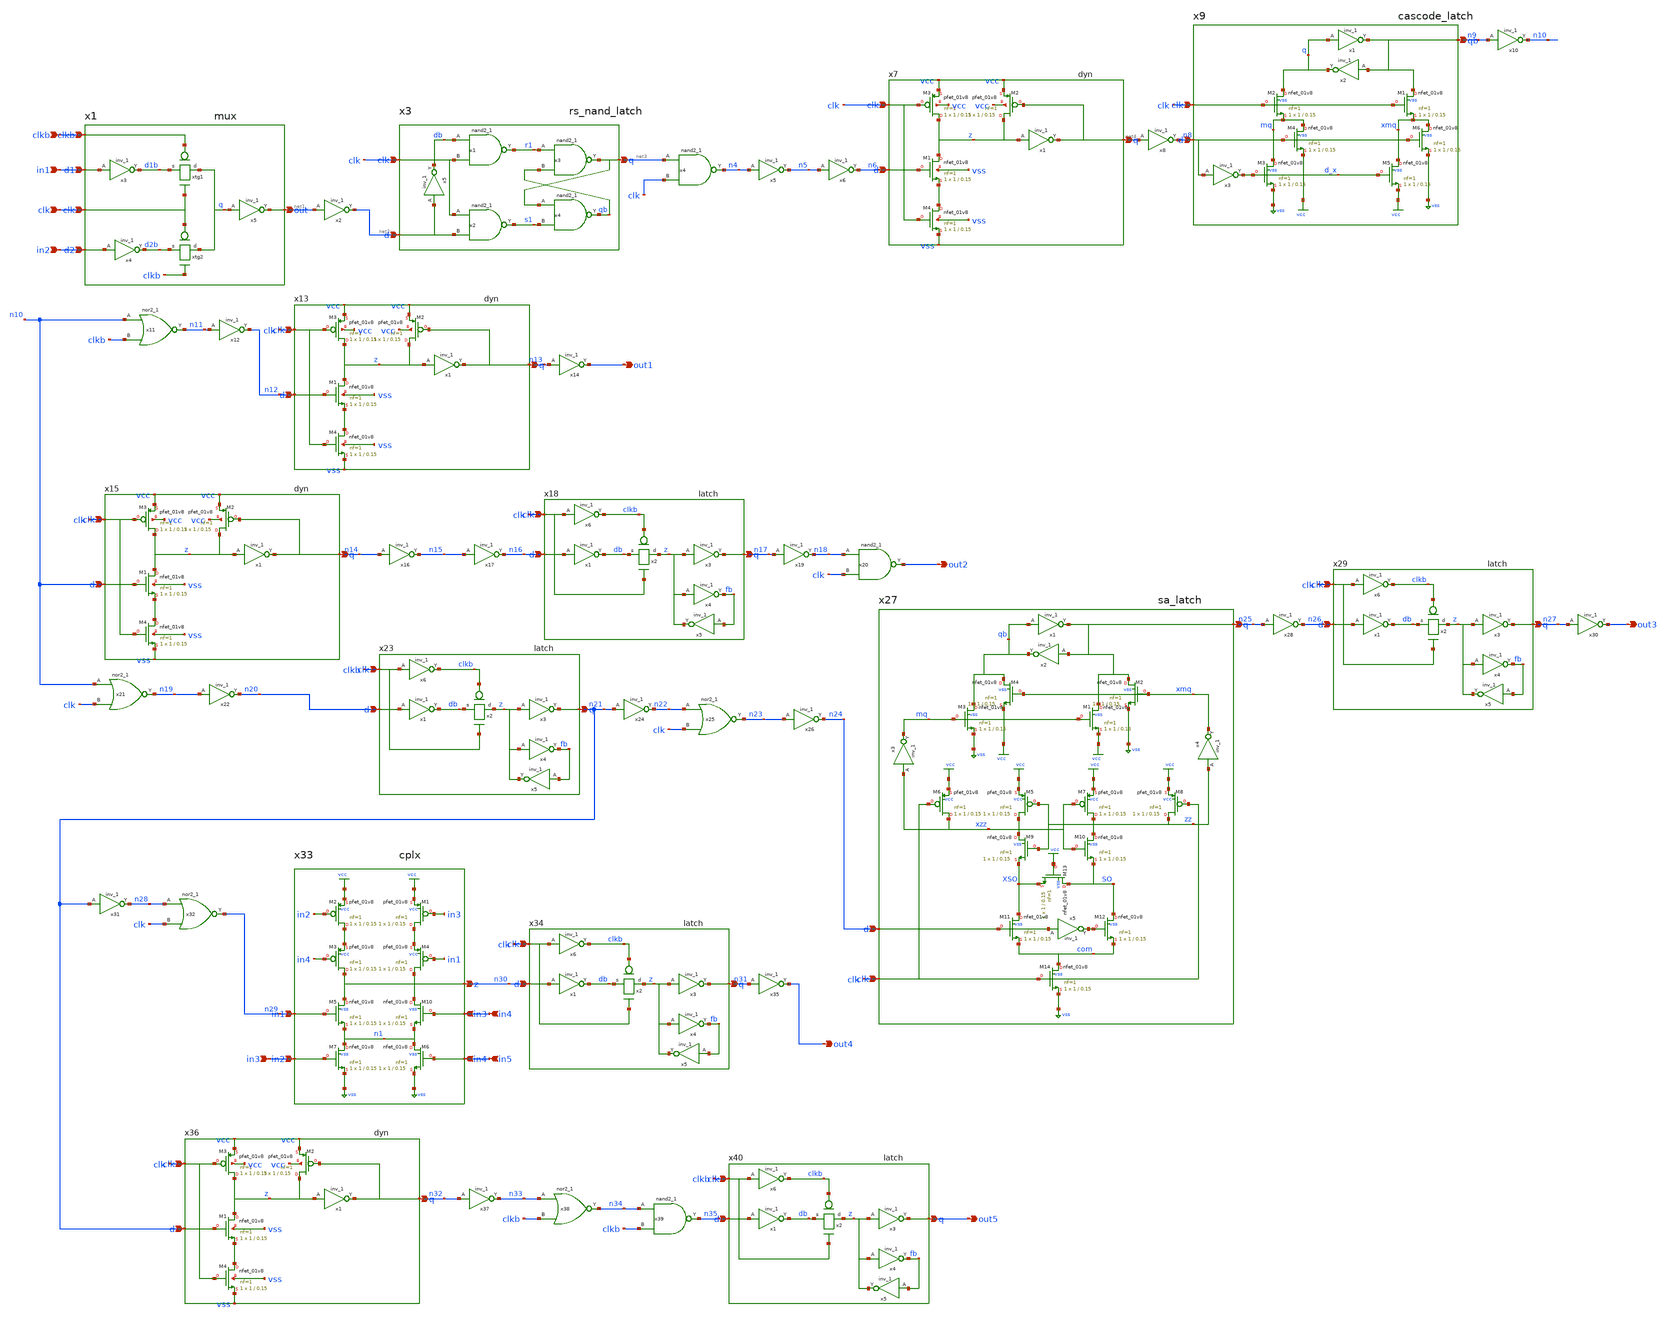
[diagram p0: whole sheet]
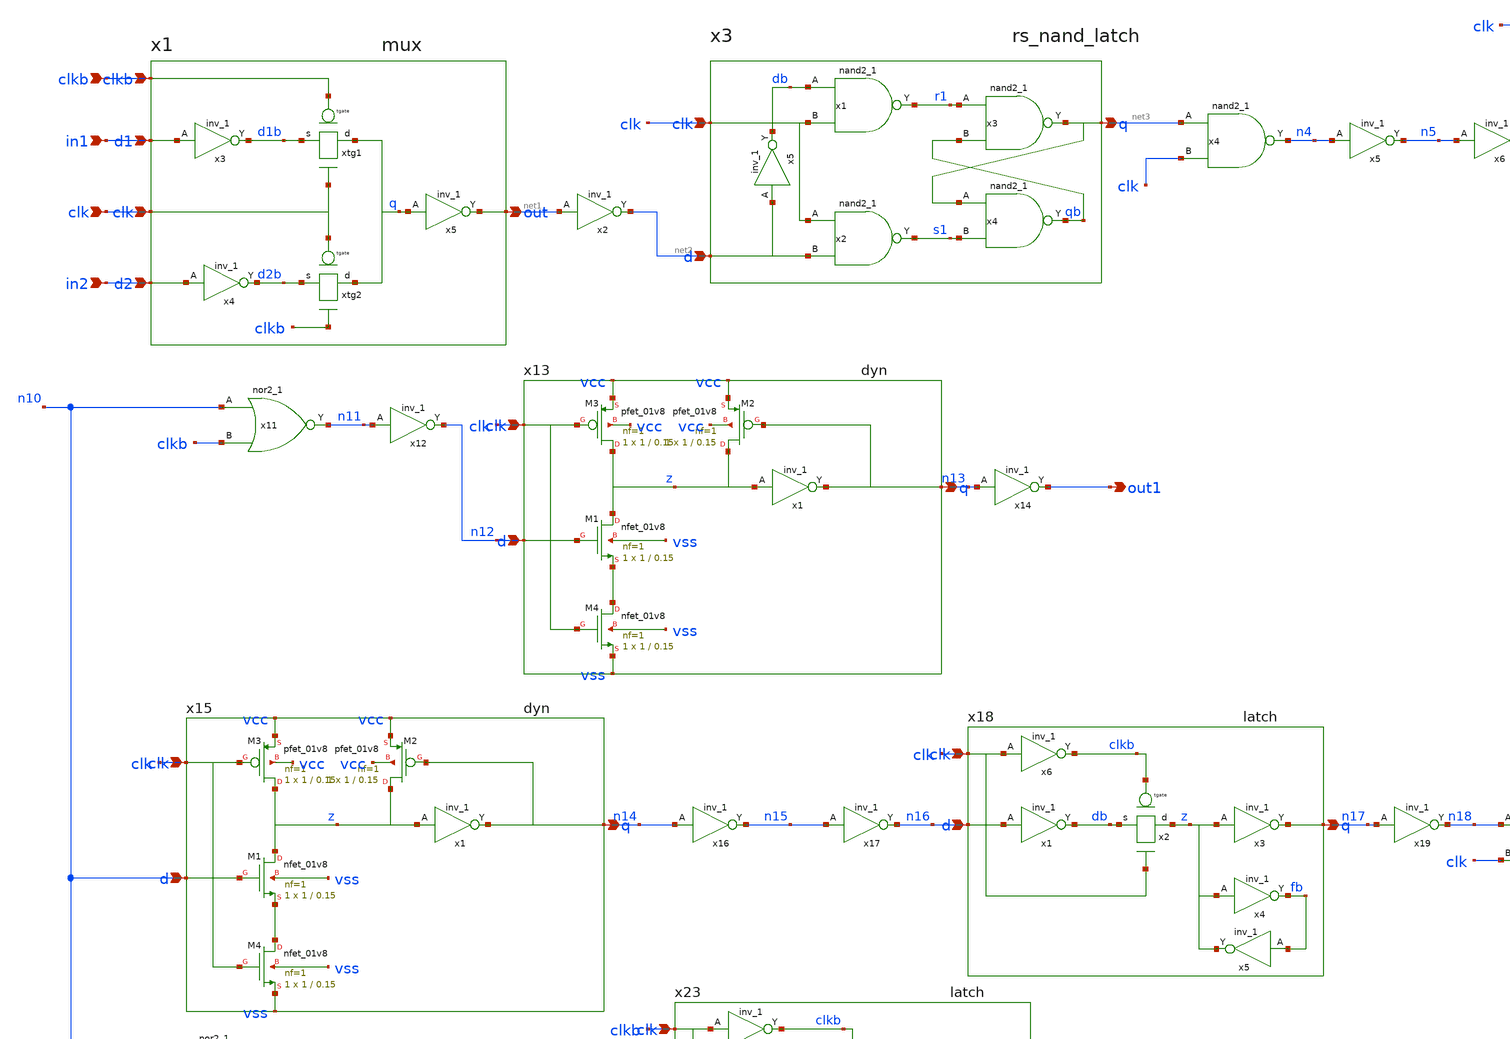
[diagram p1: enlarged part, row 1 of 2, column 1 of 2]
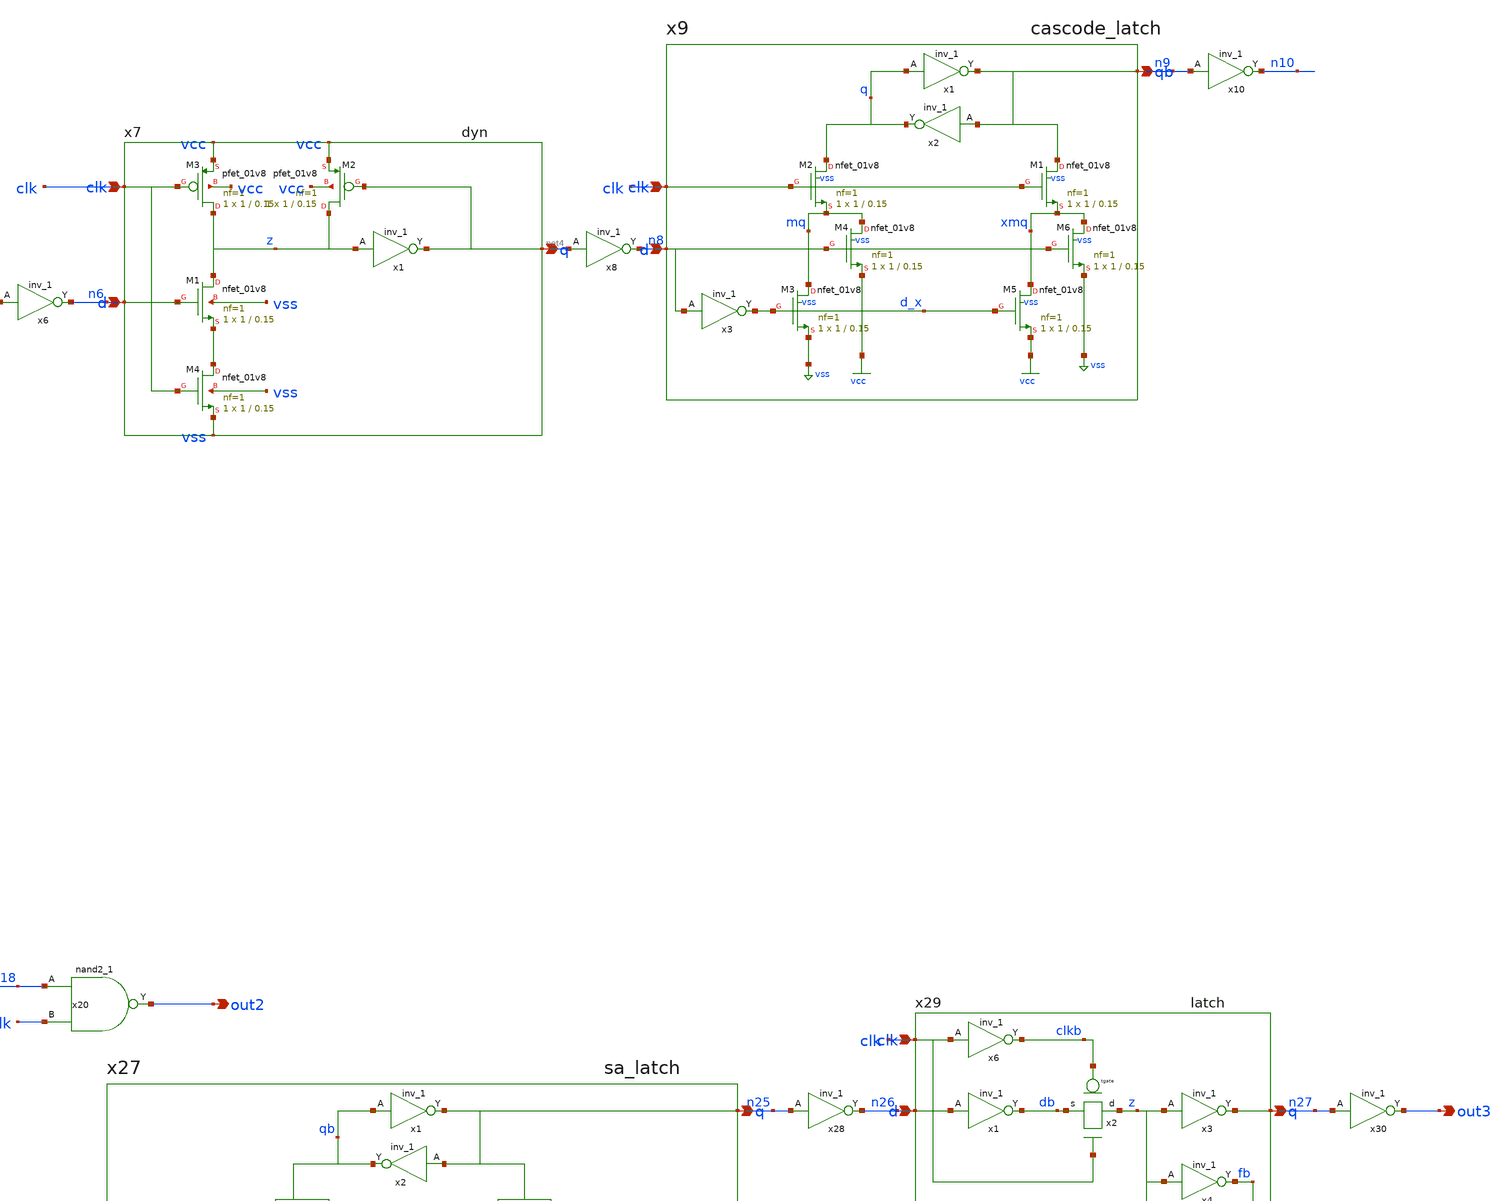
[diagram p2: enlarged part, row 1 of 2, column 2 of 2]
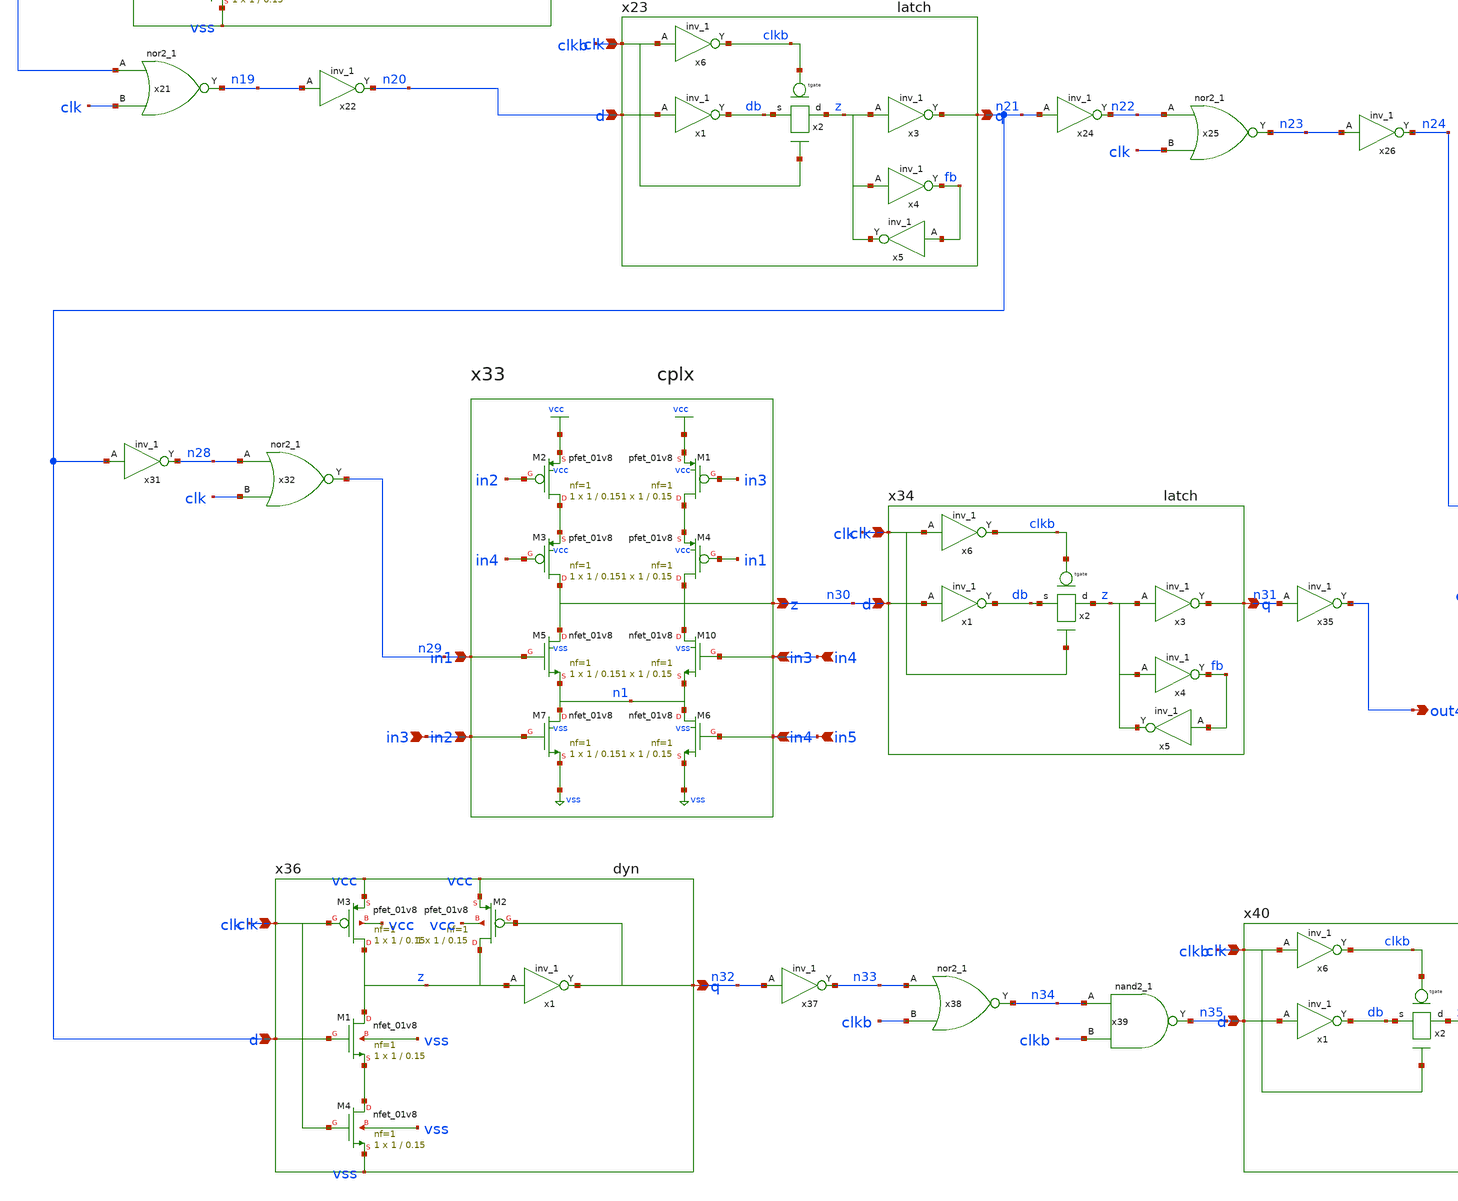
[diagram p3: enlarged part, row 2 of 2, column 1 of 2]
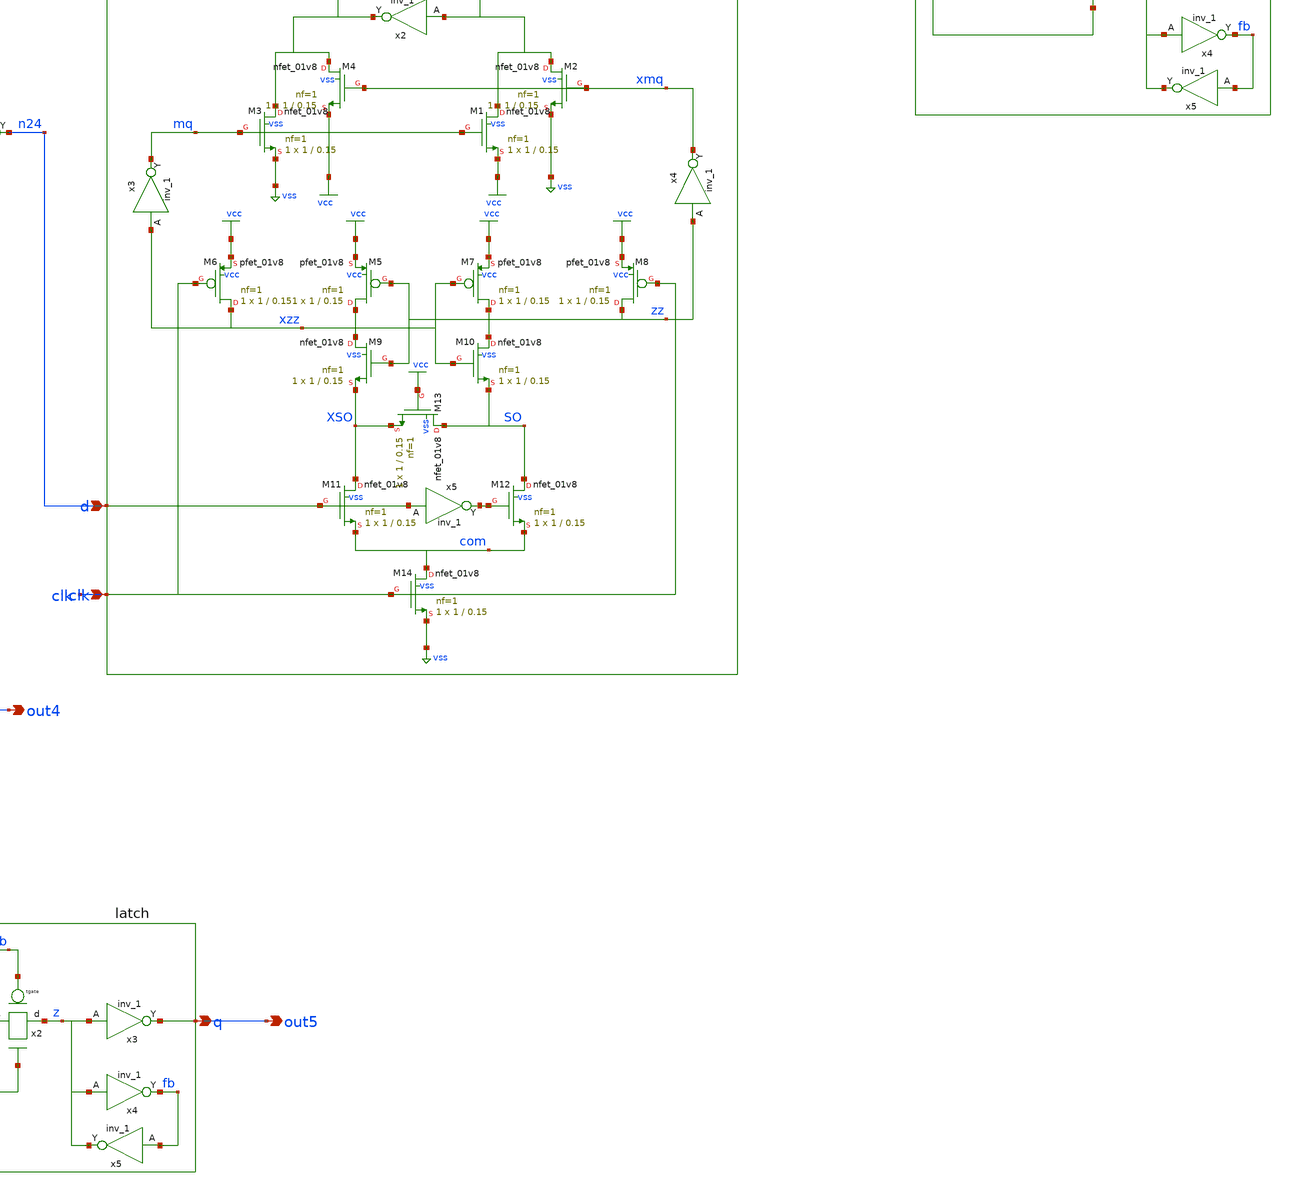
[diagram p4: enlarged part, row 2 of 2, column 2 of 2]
** sch_path: src/xe/test_cases/yxt_input_rel_test4.sch
**.subckt yxt_input_rel_test4 clkb in1 clk in2 out1 out2 out3 in3 in4 in5 out4 out5
*.ipin clkb
*.ipin in1
*.ipin clk
*.ipin in2
*.opin out1
*.opin out2
*.opin out3
*.ipin in3
*.ipin in4
*.ipin in5
*.opin out4
*.opin out5
x1 in1 in2 net1 clkb clk vcc vss mux
x2 net1 vss vss vcc vcc net2 sky130_fd_sc_hd__inv_1
x3 clk net2 net3 vcc vss rs_nand_latch
x4 net3 clk vss vss vcc vcc n4 sky130_fd_sc_hd__nand2_1
x5 n4 vss vss vcc vcc n5 sky130_fd_sc_hd__inv_1
x6 n5 vss vss vcc vcc n6 sky130_fd_sc_hd__inv_1
x7 clk net4 n6 vcc vss dyn
x8 net4 vss vss vcc vcc n8 sky130_fd_sc_hd__inv_1
x9 n8 clk n9 vcc vss cascode_latch
x10 n9 vss vss vcc vcc n10 sky130_fd_sc_hd__inv_1
x11 n10 clkb vss vss vcc vcc n11 sky130_fd_sc_hd__nor2_1
x12 n11 vss vss vcc vcc n12 sky130_fd_sc_hd__inv_1
x13 clk n13 n12 vcc vss dyn
x14 n13 vss vss vcc vcc out1 sky130_fd_sc_hd__inv_1
x15 clk n14 n10 vcc vss dyn
x16 n14 vss vss vcc vcc n15 sky130_fd_sc_hd__inv_1
x17 n15 vss vss vcc vcc n16 sky130_fd_sc_hd__inv_1
x18 clk n17 n16 vcc vss latch
x19 n17 vss vss vcc vcc n18 sky130_fd_sc_hd__inv_1
x20 n18 clk vss vss vcc vcc out2 sky130_fd_sc_hd__nand2_1
x21 n10 clk vss vss vcc vcc n19 sky130_fd_sc_hd__nor2_1
x22 n19 vss vss vcc vcc n20 sky130_fd_sc_hd__inv_1
x23 clkb n21 n20 vcc vss latch
x24 n21 vss vss vcc vcc n22 sky130_fd_sc_hd__inv_1
x25 n22 clk vss vss vcc vcc n23 sky130_fd_sc_hd__nor2_1
x26 n23 vss vss vcc vcc n24 sky130_fd_sc_hd__inv_1
x27 clk n25 n24 vcc vss sa_latch
x28 n25 vss vss vcc vcc n26 sky130_fd_sc_hd__inv_1
x29 clk n27 n26 vcc vss latch
x30 n27 vss vss vcc vcc out3 sky130_fd_sc_hd__inv_1
x33 n29 in3 in4 in5 n30 vcc vss cplx
x32 n28 clk vss vss vcc vcc n29 sky130_fd_sc_hd__nor2_1
x31 n21 vss vss vcc vcc n28 sky130_fd_sc_hd__inv_1
x34 clk n31 n30 vcc vss latch
x35 n31 vss vss vcc vcc out4 sky130_fd_sc_hd__inv_1
x36 clk n32 n21 vcc vss dyn
x37 n32 vss vss vcc vcc n33 sky130_fd_sc_hd__inv_1
x38 n33 clkb vss vss vcc vcc n34 sky130_fd_sc_hd__nor2_1
x39 n34 clkb vss vss vcc vcc n35 sky130_fd_sc_hd__nand2_1
x40 clkb out5 n35 vcc vss latch
**** begin user architecture code

** opencircuitdesign pdks install

.subckt sky130_fd_sc_hd__inv_1 A VGND VNB VPB VPWR Y
M0 VGND A Y VNB sky130_fd_pr__nfet_01v8 w=650000u l=150000u
M1 VPWR A Y VPB sky130_fd_pr__pfet_01v8_hvt w=1e+06u l=150000u
.ends

.subckt sky130_fd_sc_hd__nand2_1 A B VGND VNB VPB VPWR Y
M0 Y A VPWR VPB sky130_fd_pr__pfet_01v8_hvt w=1e+06u l=150000u
M1 VPWR B Y VPB sky130_fd_pr__pfet_01v8_hvt w=1e+06u l=150000u
M2 VGND B a_113_47# VNB sky130_fd_pr__nfet_01v8 w=650000u l=150000u
M3 a_113_47# A Y VNB sky130_fd_pr__nfet_01v8 w=650000u l=150000u
.ends

.SUBCKT sky130_fd_sc_hd__nor2_1 A B VGND VNB VPB VPWR Y
*.PININFO A:I B:I VGND:I VNB:I VPB:I VPWR:I Y:O
MMP0 VPWR A sndPA VPB sky130_fd_pr__pfet_01v8_hvt m=1 w=1.0 l=0.15 mult=1 sa=0.265  sb=0.265 sd=0.28
+ topography=normal area=0.063 perim=1.14
MMP1 sndPA B Y VPB sky130_fd_pr__pfet_01v8_hvt m=1 w=1.0 l=0.15 mult=1 sa=0.265  sb=0.265 sd=0.28
+ topography=normal area=0.063 perim=1.14
MMN0 Y A VGND VNB sky130_fd_pr__nfet_01v8 m=1 w=0.65 l=0.15 mult=1 sa=0.265 sb=0.265  sd=0.28
+ topography=normal area=0.063 perim=1.14
MMN1 Y B VGND VNB sky130_fd_pr__nfet_01v8 m=1 w=0.65 l=0.15 mult=1 sa=0.265 sb=0.265  sd=0.28
+ topography=normal area=0.063 perim=1.14
.ENDS sky130_fd_sc_hd__nor2_1


**** end user architecture code
**.ends

* expanding   symbol:  yxt/mux.sch # of pins=5
** sym_path: src/xe/test_cases/mux.sch
** sch_path: src/xe/test_cases/mux.sch
.subckt mux d1 d2 out clkb clk vcc vss
*.ipin d1
*.ipin d2
*.opin out
*.ipin clkb
*.ipin clk
xtg1 clkb d1b q clk vcc vss tgate
xtg2 clk d2b q clkb vcc vss tgate
x3 d1 vss vss vcc vcc d1b sky130_fd_sc_hd__inv_1
x4 d2 vss vss vcc vcc d2b sky130_fd_sc_hd__inv_1
x5 q vss vss vcc vcc out sky130_fd_sc_hd__inv_1
.ends


* expanding   symbol:  yxt/rs_nand_latch.sch # of pins=3
** sym_path: src/xe/test_cases/rs_nand_latch.sch
** sch_path: src/xe/test_cases/rs_nand_latch.sch
.subckt rs_nand_latch clk d q vcc vss
*.ipin clk
*.ipin d
*.opin q
x1 db clk vss vss vcc vcc r1 sky130_fd_sc_hd__nand2_1
x5 d vss vss vcc vcc db sky130_fd_sc_hd__inv_1
x2 clk d vss vss vcc vcc s1 sky130_fd_sc_hd__nand2_1
x3 r1 qb vss vss vcc vcc q sky130_fd_sc_hd__nand2_1
x4 q s1 vss vss vcc vcc qb sky130_fd_sc_hd__nand2_1
.ends


* expanding   symbol:  yxt/dyn.sch # of pins=3
** sym_path: src/xe/test_cases/dyn.sch
** sch_path: src/xe/test_cases/dyn.sch
.subckt dyn clk q d vcc vss
*.ipin clk
*.opin q
*.ipin d
x1 z vss vss vcc vcc q sky130_fd_sc_hd__inv_1
XM1 z d net1 vss sky130_fd_pr__nfet_01v8 L=0.15 W=1 nf=1 ad='int((nf+1)/2) * W/nf * 0.29' as='int((nf+2)/2) * W/nf * 0.29'
+ pd='2*int((nf+1)/2) * (W/nf + 0.29)' ps='2*int((nf+2)/2) * (W/nf + 0.29)' nrd='0.29 / W' nrs='0.29 / W'
+ sa=0 sb=0 sd=0 mult=1 m=1
XM2 z q vcc vcc sky130_fd_pr__pfet_01v8 L=0.15 W=1 nf=1 ad='int((nf+1)/2) * W/nf * 0.29' as='int((nf+2)/2) * W/nf * 0.29'
+ pd='2*int((nf+1)/2) * (W/nf + 0.29)' ps='2*int((nf+2)/2) * (W/nf + 0.29)' nrd='0.29 / W' nrs='0.29 / W'
+ sa=0 sb=0 sd=0 mult=1 m=1
XM3 z clk vcc vcc sky130_fd_pr__pfet_01v8 L=0.15 W=1 nf=1 ad='int((nf+1)/2) * W/nf * 0.29' as='int((nf+2)/2) * W/nf * 0.29'
+ pd='2*int((nf+1)/2) * (W/nf + 0.29)' ps='2*int((nf+2)/2) * (W/nf + 0.29)' nrd='0.29 / W' nrs='0.29 / W'
+ sa=0 sb=0 sd=0 mult=1 m=1
XM4 net1 clk vss vss sky130_fd_pr__nfet_01v8 L=0.15 W=1 nf=1 ad='int((nf+1)/2) * W/nf * 0.29' as='int((nf+2)/2) * W/nf * 0.29'
+ pd='2*int((nf+1)/2) * (W/nf + 0.29)' ps='2*int((nf+2)/2) * (W/nf + 0.29)' nrd='0.29 / W' nrs='0.29 / W'
+ sa=0 sb=0 sd=0 mult=1 m=1
.ends


* expanding   symbol:  yxt/cascode_latch.sch # of pins=3
** sym_path: src/xe/test_cases/cascode_latch.sch
** sch_path: src/xe/test_cases/cascode_latch.sch
.subckt cascode_latch d clk qb vcc vss
*.ipin d
*.ipin clk
*.opin qb
x1 q vss vss vcc vcc qb sky130_fd_sc_hd__inv_1
x2 qb vss vss vcc vcc q sky130_fd_sc_hd__inv_1
XM1 qb clk xmq vss sky130_fd_pr__nfet_01v8 L=0.15 W=1 nf=1 ad='int((nf+1)/2) * W/nf * 0.29' as='int((nf+2)/2) * W/nf * 0.29'
+ pd='2*int((nf+1)/2) * (W/nf + 0.29)' ps='2*int((nf+2)/2) * (W/nf + 0.29)' nrd='0.29 / W' nrs='0.29 / W'
+ sa=0 sb=0 sd=0 mult=1 m=1
XM2 q clk mq vss sky130_fd_pr__nfet_01v8 L=0.15 W=1 nf=1 ad='int((nf+1)/2) * W/nf * 0.29' as='int((nf+2)/2) * W/nf * 0.29'
+ pd='2*int((nf+1)/2) * (W/nf + 0.29)' ps='2*int((nf+2)/2) * (W/nf + 0.29)' nrd='0.29 / W' nrs='0.29 / W'
+ sa=0 sb=0 sd=0 mult=1 m=1
XM3 mq d_x vss vss sky130_fd_pr__nfet_01v8 L=0.15 W=1 nf=1 ad='int((nf+1)/2) * W/nf * 0.29' as='int((nf+2)/2) * W/nf * 0.29'
+ pd='2*int((nf+1)/2) * (W/nf + 0.29)' ps='2*int((nf+2)/2) * (W/nf + 0.29)' nrd='0.29 / W' nrs='0.29 / W'
+ sa=0 sb=0 sd=0 mult=1 m=1
XM4 mq d vcc vss sky130_fd_pr__nfet_01v8 L=0.15 W=1 nf=1 ad='int((nf+1)/2) * W/nf * 0.29' as='int((nf+2)/2) * W/nf * 0.29'
+ pd='2*int((nf+1)/2) * (W/nf + 0.29)' ps='2*int((nf+2)/2) * (W/nf + 0.29)' nrd='0.29 / W' nrs='0.29 / W'
+ sa=0 sb=0 sd=0 mult=1 m=1
XM5 xmq d_x vcc vss sky130_fd_pr__nfet_01v8 L=0.15 W=1 nf=1 ad='int((nf+1)/2) * W/nf * 0.29' as='int((nf+2)/2) * W/nf * 0.29'
+ pd='2*int((nf+1)/2) * (W/nf + 0.29)' ps='2*int((nf+2)/2) * (W/nf + 0.29)' nrd='0.29 / W' nrs='0.29 / W'
+ sa=0 sb=0 sd=0 mult=1 m=1
XM6 xmq d vss vss sky130_fd_pr__nfet_01v8 L=0.15 W=1 nf=1 ad='int((nf+1)/2) * W/nf * 0.29' as='int((nf+2)/2) * W/nf * 0.29'
+ pd='2*int((nf+1)/2) * (W/nf + 0.29)' ps='2*int((nf+2)/2) * (W/nf + 0.29)' nrd='0.29 / W' nrs='0.29 / W'
+ sa=0 sb=0 sd=0 mult=1 m=1
x3 d vss vss vcc vcc d_x sky130_fd_sc_hd__inv_1
.ends


* expanding   symbol:  yxt/latch.sch # of pins=3
** sym_path: src/xe/test_cases/latch.sch
** sch_path: src/xe/test_cases/latch.sch
.subckt latch clk q d vcc vss
*.ipin clk
*.ipin d
*.opin q
x1 d vss vss vcc vcc db sky130_fd_sc_hd__inv_1
x2 clkb db z clk vcc vss tgate
x3 z vss vss vcc vcc q sky130_fd_sc_hd__inv_1
x6 clk vss vss vcc vcc clkb sky130_fd_sc_hd__inv_1
x4 z vss vss vcc vcc fb sky130_fd_sc_hd__inv_1
x5 fb vss vss vcc vcc z sky130_fd_sc_hd__inv_1
.ends


* expanding   symbol:  yxt/sa_latch.sch # of pins=3
** sym_path: src/xe/test_cases/sa_latch.sch
** sch_path: src/xe/test_cases/sa_latch.sch
.subckt sa_latch clk q d vcc vss
*.ipin clk
*.opin q
*.ipin d
x1 qb vss vss vcc vcc q sky130_fd_sc_hd__inv_1
x2 q vss vss vcc vcc qb sky130_fd_sc_hd__inv_1
XM3 qb mq vss vss sky130_fd_pr__nfet_01v8 L=0.15 W=1 nf=1 ad='int((nf+1)/2) * W/nf * 0.29' as='int((nf+2)/2) * W/nf * 0.29'
+ pd='2*int((nf+1)/2) * (W/nf + 0.29)' ps='2*int((nf+2)/2) * (W/nf + 0.29)' nrd='0.29 / W' nrs='0.29 / W'
+ sa=0 sb=0 sd=0 mult=1 m=1
XM4 qb xmq vcc vss sky130_fd_pr__nfet_01v8 L=0.15 W=1 nf=1 ad='int((nf+1)/2) * W/nf * 0.29' as='int((nf+2)/2) * W/nf * 0.29'
+ pd='2*int((nf+1)/2) * (W/nf + 0.29)' ps='2*int((nf+2)/2) * (W/nf + 0.29)' nrd='0.29 / W' nrs='0.29 / W'
+ sa=0 sb=0 sd=0 mult=1 m=1
XM1 q mq vcc vss sky130_fd_pr__nfet_01v8 L=0.15 W=1 nf=1 ad='int((nf+1)/2) * W/nf * 0.29' as='int((nf+2)/2) * W/nf * 0.29'
+ pd='2*int((nf+1)/2) * (W/nf + 0.29)' ps='2*int((nf+2)/2) * (W/nf + 0.29)' nrd='0.29 / W' nrs='0.29 / W'
+ sa=0 sb=0 sd=0 mult=1 m=1
XM2 q xmq vss vss sky130_fd_pr__nfet_01v8 L=0.15 W=1 nf=1 ad='int((nf+1)/2) * W/nf * 0.29' as='int((nf+2)/2) * W/nf * 0.29'
+ pd='2*int((nf+1)/2) * (W/nf + 0.29)' ps='2*int((nf+2)/2) * (W/nf + 0.29)' nrd='0.29 / W' nrs='0.29 / W'
+ sa=0 sb=0 sd=0 mult=1 m=1
x3 xzz vss vss vcc vcc mq sky130_fd_sc_hd__inv_1
x4 zz vss vss vcc vcc xmq sky130_fd_sc_hd__inv_1
XM5 xzz zz vcc vcc sky130_fd_pr__pfet_01v8 L=0.15 W=1 nf=1 ad='int((nf+1)/2) * W/nf * 0.29' as='int((nf+2)/2) * W/nf * 0.29'
+ pd='2*int((nf+1)/2) * (W/nf + 0.29)' ps='2*int((nf+2)/2) * (W/nf + 0.29)' nrd='0.29 / W' nrs='0.29 / W'
+ sa=0 sb=0 sd=0 mult=1 m=1
XM6 xzz clk vcc vcc sky130_fd_pr__pfet_01v8 L=0.15 W=1 nf=1 ad='int((nf+1)/2) * W/nf * 0.29' as='int((nf+2)/2) * W/nf * 0.29'
+ pd='2*int((nf+1)/2) * (W/nf + 0.29)' ps='2*int((nf+2)/2) * (W/nf + 0.29)' nrd='0.29 / W' nrs='0.29 / W'
+ sa=0 sb=0 sd=0 mult=1 m=1
XM7 zz xzz vcc vcc sky130_fd_pr__pfet_01v8 L=0.15 W=1 nf=1 ad='int((nf+1)/2) * W/nf * 0.29' as='int((nf+2)/2) * W/nf * 0.29'
+ pd='2*int((nf+1)/2) * (W/nf + 0.29)' ps='2*int((nf+2)/2) * (W/nf + 0.29)' nrd='0.29 / W' nrs='0.29 / W'
+ sa=0 sb=0 sd=0 mult=1 m=1
XM8 zz clk vcc vcc sky130_fd_pr__pfet_01v8 L=0.15 W=1 nf=1 ad='int((nf+1)/2) * W/nf * 0.29' as='int((nf+2)/2) * W/nf * 0.29'
+ pd='2*int((nf+1)/2) * (W/nf + 0.29)' ps='2*int((nf+2)/2) * (W/nf + 0.29)' nrd='0.29 / W' nrs='0.29 / W'
+ sa=0 sb=0 sd=0 mult=1 m=1
XM9 xzz zz XSO vss sky130_fd_pr__nfet_01v8 L=0.15 W=1 nf=1 ad='int((nf+1)/2) * W/nf * 0.29' as='int((nf+2)/2) * W/nf * 0.29'
+ pd='2*int((nf+1)/2) * (W/nf + 0.29)' ps='2*int((nf+2)/2) * (W/nf + 0.29)' nrd='0.29 / W' nrs='0.29 / W'
+ sa=0 sb=0 sd=0 mult=1 m=1
XM10 zz xzz SO vss sky130_fd_pr__nfet_01v8 L=0.15 W=1 nf=1 ad='int((nf+1)/2) * W/nf * 0.29' as='int((nf+2)/2) * W/nf * 0.29'
+ pd='2*int((nf+1)/2) * (W/nf + 0.29)' ps='2*int((nf+2)/2) * (W/nf + 0.29)' nrd='0.29 / W' nrs='0.29 / W'
+ sa=0 sb=0 sd=0 mult=1 m=1
XM11 XSO d com vss sky130_fd_pr__nfet_01v8 L=0.15 W=1 nf=1 ad='int((nf+1)/2) * W/nf * 0.29' as='int((nf+2)/2) * W/nf * 0.29'
+ pd='2*int((nf+1)/2) * (W/nf + 0.29)' ps='2*int((nf+2)/2) * (W/nf + 0.29)' nrd='0.29 / W' nrs='0.29 / W'
+ sa=0 sb=0 sd=0 mult=1 m=1
XM12 SO net1 com vss sky130_fd_pr__nfet_01v8 L=0.15 W=1 nf=1 ad='int((nf+1)/2) * W/nf * 0.29' as='int((nf+2)/2) * W/nf * 0.29'
+ pd='2*int((nf+1)/2) * (W/nf + 0.29)' ps='2*int((nf+2)/2) * (W/nf + 0.29)' nrd='0.29 / W' nrs='0.29 / W'
+ sa=0 sb=0 sd=0 mult=1 m=1
XM13 SO vcc XSO vss sky130_fd_pr__nfet_01v8 L=0.15 W=1 nf=1 ad='int((nf+1)/2) * W/nf * 0.29' as='int((nf+2)/2) * W/nf * 0.29'
+ pd='2*int((nf+1)/2) * (W/nf + 0.29)' ps='2*int((nf+2)/2) * (W/nf + 0.29)' nrd='0.29 / W' nrs='0.29 / W'
+ sa=0 sb=0 sd=0 mult=1 m=1
x5 d vss vss vcc vcc net1 sky130_fd_sc_hd__inv_1
XM14 com clk vss vss sky130_fd_pr__nfet_01v8 L=0.15 W=1 nf=1 ad='int((nf+1)/2) * W/nf * 0.29' as='int((nf+2)/2) * W/nf * 0.29'
+ pd='2*int((nf+1)/2) * (W/nf + 0.29)' ps='2*int((nf+2)/2) * (W/nf + 0.29)' nrd='0.29 / W' nrs='0.29 / W'
+ sa=0 sb=0 sd=0 mult=1 m=1
.ends


* expanding   symbol:  yxt/cplx.sch # of pins=5
** sym_path: src/xe/test_cases/cplx.sch
** sch_path: src/xe/test_cases/cplx.sch
.subckt cplx in1 in2 in3 in4 z vcc vss
*.ipin in1
*.ipin in2
*.ipin in3
*.ipin in4
*.opin z
XM2 net1 in2 vcc vcc sky130_fd_pr__pfet_01v8 L=0.15 W=1 nf=1 ad='int((nf+1)/2) * W/nf * 0.29' as='int((nf+2)/2) * W/nf * 0.29'
+ pd='2*int((nf+1)/2) * (W/nf + 0.29)' ps='2*int((nf+2)/2) * (W/nf + 0.29)' nrd='0.29 / W' nrs='0.29 / W'
+ sa=0 sb=0 sd=0 mult=1 m=1
XM10 z in3 n1 vss sky130_fd_pr__nfet_01v8 L=0.15 W=1 nf=1 ad='int((nf+1)/2) * W/nf * 0.29' as='int((nf+2)/2) * W/nf * 0.29'
+ pd='2*int((nf+1)/2) * (W/nf + 0.29)' ps='2*int((nf+2)/2) * (W/nf + 0.29)' nrd='0.29 / W' nrs='0.29 / W'
+ sa=0 sb=0 sd=0 mult=1 m=1
XM1 net2 in3 vcc vcc sky130_fd_pr__pfet_01v8 L=0.15 W=1 nf=1 ad='int((nf+1)/2) * W/nf * 0.29' as='int((nf+2)/2) * W/nf * 0.29'
+ pd='2*int((nf+1)/2) * (W/nf + 0.29)' ps='2*int((nf+2)/2) * (W/nf + 0.29)' nrd='0.29 / W' nrs='0.29 / W'
+ sa=0 sb=0 sd=0 mult=1 m=1
XM3 z in4 net1 vcc sky130_fd_pr__pfet_01v8 L=0.15 W=1 nf=1 ad='int((nf+1)/2) * W/nf * 0.29' as='int((nf+2)/2) * W/nf * 0.29'
+ pd='2*int((nf+1)/2) * (W/nf + 0.29)' ps='2*int((nf+2)/2) * (W/nf + 0.29)' nrd='0.29 / W' nrs='0.29 / W'
+ sa=0 sb=0 sd=0 mult=1 m=1
XM4 z in1 net2 vcc sky130_fd_pr__pfet_01v8 L=0.15 W=1 nf=1 ad='int((nf+1)/2) * W/nf * 0.29' as='int((nf+2)/2) * W/nf * 0.29'
+ pd='2*int((nf+1)/2) * (W/nf + 0.29)' ps='2*int((nf+2)/2) * (W/nf + 0.29)' nrd='0.29 / W' nrs='0.29 / W'
+ sa=0 sb=0 sd=0 mult=1 m=1
XM5 z in1 n1 vss sky130_fd_pr__nfet_01v8 L=0.15 W=1 nf=1 ad='int((nf+1)/2) * W/nf * 0.29' as='int((nf+2)/2) * W/nf * 0.29'
+ pd='2*int((nf+1)/2) * (W/nf + 0.29)' ps='2*int((nf+2)/2) * (W/nf + 0.29)' nrd='0.29 / W' nrs='0.29 / W'
+ sa=0 sb=0 sd=0 mult=1 m=1
XM6 n1 in4 vss vss sky130_fd_pr__nfet_01v8 L=0.15 W=1 nf=1 ad='int((nf+1)/2) * W/nf * 0.29' as='int((nf+2)/2) * W/nf * 0.29'
+ pd='2*int((nf+1)/2) * (W/nf + 0.29)' ps='2*int((nf+2)/2) * (W/nf + 0.29)' nrd='0.29 / W' nrs='0.29 / W'
+ sa=0 sb=0 sd=0 mult=1 m=1
XM7 n1 in2 vss vss sky130_fd_pr__nfet_01v8 L=0.15 W=1 nf=1 ad='int((nf+1)/2) * W/nf * 0.29' as='int((nf+2)/2) * W/nf * 0.29'
+ pd='2*int((nf+1)/2) * (W/nf + 0.29)' ps='2*int((nf+2)/2) * (W/nf + 0.29)' nrd='0.29 / W' nrs='0.29 / W'
+ sa=0 sb=0 sd=0 mult=1 m=1
.ends


* expanding   symbol:  yxt/tgate.sym # of pins=4
** sym_path: src/xe/test_cases/tgate.sym
** sch_path: src/xe/test_cases/tgate.sch
.subckt tgate gp s d gn vcc vss
*.ipin s
*.ipin gp
*.ipin gn
*.opin d
XMpc d gp s vss sky130_fd_pr__pfet_01v8 L=0.15 W=1 nf=1 ad='int((nf+1)/2) * W/nf * 0.29' as='int((nf+2)/2) * W/nf * 0.29'
+ pd='2*int((nf+1)/2) * (W/nf + 0.29)' ps='2*int((nf+2)/2) * (W/nf + 0.29)' nrd='0.29 / W' nrs='0.29 / W'
+ sa=0 sb=0 sd=0 mult=7 m=7
XM15 s gn d vcc sky130_fd_pr__nfet_01v8 L=0.15 W=1 nf=1 ad='int((nf+1)/2) * W/nf * 0.29' as='int((nf+2)/2) * W/nf * 0.29'
+ pd='2*int((nf+1)/2) * (W/nf + 0.29)' ps='2*int((nf+2)/2) * (W/nf + 0.29)' nrd='0.29 / W' nrs='0.29 / W'
+ sa=0 sb=0 sd=0 mult=1 m=1
.ends

.GLOBAL vcc
.GLOBAL vss
.end
